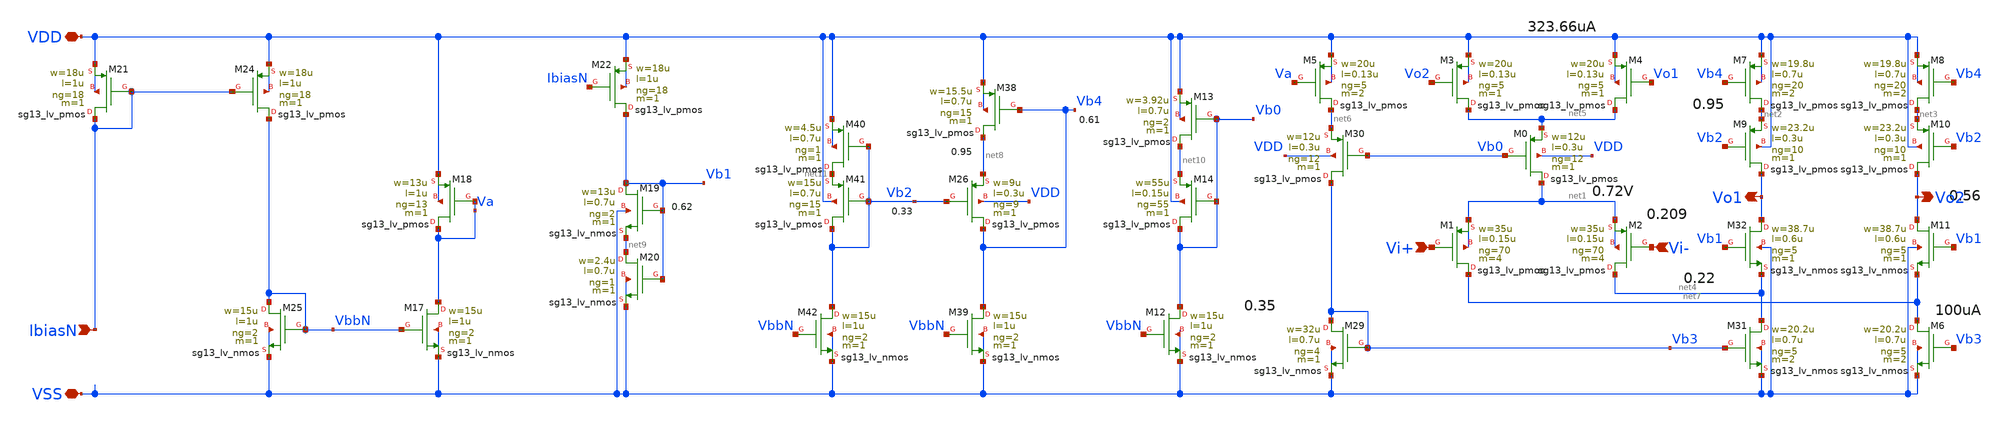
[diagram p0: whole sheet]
** sch_path: sch/blocks/gmBoosting.sch
**.subckt gmBoosting VSS Vo1 Vo2 Vi+ Vi- VDD IbiasN
*.iopin VSS
*.opin Vo1
*.opin Vo2
*.ipin Vi+
*.ipin Vi-
*.iopin VDD
*.ipin IbiasN
XM7 net2 Vb4 VDD VDD sg13_lv_pmos w=19.8u l=0.7u ng=20 m=2 mm_ok=1
XM1 net7 Vi+ net1 net1 sg13_lv_pmos w=35u l=0.15u ng=70 m=4 mm_ok=1
XM2 net4 Vi- net1 net1 sg13_lv_pmos w=35u l=0.15u ng=70 m=4 mm_ok=1
XM0 net1 Vb0 net5 VDD sg13_lv_pmos w=12u l=0.3u ng=12 m=1 mm_ok=1
XM6 net7 Vb3 VSS VSS sg13_lv_nmos w=20.2u l=0.7u ng=5 m=2 mm_ok=1
XM9 Vo1 Vb2 net2 VDD sg13_lv_pmos w=23.2u l=0.3u ng=10 m=1 mm_ok=1
XM10 Vo2 Vb2 net3 VDD sg13_lv_pmos w=23.2u l=0.3u ng=10 m=1 mm_ok=1
XM3 net5 Vo2 VDD VDD sg13_lv_pmos w=20u l=0.13u ng=5 m=1 mm_ok=1
XM4 net5 Vo1 VDD VDD sg13_lv_pmos w=20u l=0.13u ng=5 m=1 mm_ok=1
XM5 net6 Va VDD VDD sg13_lv_pmos w=20u l=0.13u ng=5 m=2 mm_ok=1
XM29 Vb3 Vb3 VSS VSS sg13_lv_nmos w=32u l=0.7u ng=4 m=1 mm_ok=1
XM30 Vb3 Vb0 net6 VDD sg13_lv_pmos w=12u l=0.3u ng=12 m=1 mm_ok=1
XM31 net4 Vb3 VSS VSS sg13_lv_nmos w=20.2u l=0.7u ng=5 m=2 mm_ok=1
XM32 Vo1 Vb1 net4 VSS sg13_lv_nmos w=38.7u l=0.6u ng=5 m=1 mm_ok=1
XM21 IbiasN IbiasN VDD VDD sg13_lv_pmos w=18u l=1u ng=18 m=1 mm_ok=1
XM24 VbbN IbiasN VDD VDD sg13_lv_pmos w=18u l=1u ng=18 m=1 mm_ok=1
XM25 VbbN VbbN VSS VSS sg13_lv_nmos w=15u l=1u ng=2 m=1 mm_ok=1
XM17 Va VbbN VSS VSS sg13_lv_nmos w=15u l=1u ng=2 m=1 mm_ok=1
XM18 Va Va VDD VDD sg13_lv_pmos w=13u l=1u ng=13 m=1 mm_ok=1
XM19 Vb1 Vb1 net9 VSS sg13_lv_nmos w=13u l=0.7u ng=2 m=1 mm_ok=1
XM20 net9 Vb1 VSS VSS sg13_lv_nmos w=2.4u l=0.7u ng=1 m=1 mm_ok=1
XM22 Vb1 IbiasN VDD VDD sg13_lv_pmos w=18u l=1u ng=18 m=1 mm_ok=1
XM26 Vb4 Vb2 net8 VDD sg13_lv_pmos w=9u l=0.3u ng=9 m=1 mm_ok=1
XM38 net8 Vb4 VDD VDD sg13_lv_pmos w=15.5u l=0.7u ng=15 m=1 mm_ok=1
XM39 Vb4 VbbN VSS VSS sg13_lv_nmos w=15u l=1u ng=2 m=1 mm_ok=1
XM40 net11 Vb2 VDD VDD sg13_lv_pmos w=4.5u l=0.7u ng=1 m=1 mm_ok=1
XM41 Vb2 Vb2 net11 VDD sg13_lv_pmos w=15u l=0.7u ng=15 m=1 mm_ok=1
XM42 Vb2 VbbN VSS VSS sg13_lv_nmos w=15u l=1u ng=2 m=1 mm_ok=1
XM8 net3 Vb4 VDD VDD sg13_lv_pmos w=19.8u l=0.7u ng=20 m=2 mm_ok=1
XM11 Vo2 Vb1 net7 VSS sg13_lv_nmos w=38.7u l=0.6u ng=5 m=1 mm_ok=1
XM12 Vb0 VbbN VSS VSS sg13_lv_nmos w=15u l=1u ng=2 m=1 mm_ok=1
XM13 net10 Vb0 VDD VDD sg13_lv_pmos w=3.92u l=0.7u ng=2 m=1 mm_ok=1
XM14 Vb0 Vb0 net10 VDD sg13_lv_pmos w=55u l=0.15u ng=55 m=1 mm_ok=1
**.ends
.end
